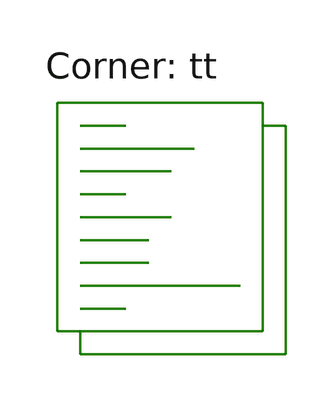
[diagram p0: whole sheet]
** sch_path: xschem/test_vref01_extracted.sch
**.subckt test_vref01_extracted
**** begin user architecture code
.lib $::SKYWATER_MODELS/sky130.lib.spice tt
**** end user architecture code
**.ends
**** begin user architecture code


** this experimental option enables mos model bin
** selection based on W/NF instead of W
*.option wnflag=1 savecurrents
.option gmin=1e-16 reltol=1e-3 vntol=1e-4 abstol=1e-16

X0 GND a_n354_1346.t6 VREF GND sky130_fd_pr__nfet_01v8 ad=0.238 pd=2.22 as=0.238 ps=2.22 w=0.82
+ l=1.05
X1 DD.t1 a_n354_1346.t0 a_n354_1346.t1 GND sky130_fd_pr__nfet_01v8_lvt ad=1.74 pd=12.6 as=1.74
+ ps=12.6 w=6 l=0.89
X2 VREF a_n354_1346.t4 a_n354_1346.t5 GND sky130_fd_pr__nfet_01v8_lvt ad=0.499 pd=4.02 as=0.499
+ ps=4.02 w=1.72 l=3.1
X3 DD.t0 a_n354_1346.t2 a_n354_1346.t3 GND sky130_fd_pr__nfet_01v8_lvt ad=1.74 pd=12.6 as=1.74
+ ps=12.6 w=6 l=0.89
D0 VREF DD.t2 sky130_fd_pr__diode_pd2nw_05v5_lvt pj=2.6e+06 area=4.225e+11
R0 a_n354_1346.n0 a_n354_1346.t0 177.476
R1 a_n354_1346.n0 a_n354_1346.t2 177.371
R2 a_n354_1346.n6 a_n354_1346.t6 31.4497
R3 a_n354_1346.n1 a_n354_1346.t4 17.6491
R4 a_n354_1346.n4 a_n354_1346.t5 10.2714
R5 a_n354_1346.t1 a_n354_1346.n0 4.93845
R6 a_n354_1346.n1 a_n354_1346.t3 2.90106
R7 a_n354_1346.n6 a_n354_1346.n1 0.941548
R8 a_n354_1346.n4 a_n354_1346.n3 0.923627
R9 a_n354_1346.n1 a_n354_1346.n5 0.836115
R10 a_n354_1346.n5 a_n354_1346.n2 0.773938
R11 a_n354_1346.n0 a_n354_1346.n6 0.385713
R12 a_n354_1346.n5 a_n354_1346.n4 0.224162
R13 DD.t2 DD.n1 475
R14 DD.n2 DD.t2 330
R15 DD.n6 DD.n5 9.3005
R16 DD DD.t0 4.82324
R17 DD.n7 DD.t1 4.3481
R18 DD.n3 DD.n2 2.84494
R19 DD.n4 DD.n0 2.8192
R20 DD.n7 DD.n6 2.65834
R21 DD DD.n7 0.219678
R22 DD.n6 DD.n4 0.115443
R23 DD.n4 DD.n3 0.00051539
C0 VREF DD 0.42f
C1 VREF GND 1.2f
C2 DD GND 3.13f
C3 DD.t1 GND 0.154f
C4 DD.n0 GND 0.0541f
C5 DD.n1 GND 0.11f
C6 DD.t2 GND 0.187f
C7 DD.n2 GND 0.319f
C8 DD.n3 GND 0.00946f
C9 DD.n4 GND 0.0379f
C10 DD.n5 GND 0.0576f
C11 DD.n6 GND 0.151f
C12 DD.n7 GND 0.483f
C13 DD.t0 GND 0.179f
C14 a_n354_1346.n0 GND 0.448f
C15 a_n354_1346.n1 GND 0.342f
C16 a_n354_1346.t0 GND 0.125f
C17 a_n354_1346.t2 GND 0.124f
C18 a_n354_1346.t6 GND 0.0336f
C19 a_n354_1346.t4 GND 0.15f
C20 a_n354_1346.t3 GND 0.0185f
C21 a_n354_1346.n2 GND 0.239f
C22 a_n354_1346.n3 GND 0.278f
C23 a_n354_1346.t5 GND 0.00593f
C24 a_n354_1346.n4 GND 0.12f
C25 a_n354_1346.n5 GND 0.0463f
C26 a_n354_1346.n6 GND 0.0907f
C27 a_n354_1346.t1 GND 0.0795f

.param vdd=1
v1 dd 0 dc=vdd

.control
  option seed = 8
  let run = 1
  save all
  op
  write test_vref01_ext.raw
  reset
  set appendwrite
  dowhile run < = 1
    save vref i(v1)
    * save all
    dc temp -40 150 1
    write test_vref01_ext.raw
    let run = run + 1
    reset
  end
  plot v(vref)
.endc


**** end user architecture code
.end
